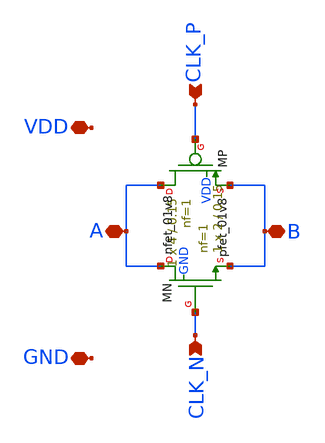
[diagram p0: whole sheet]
** sch_path: blocks/05_Switch_Network/xschem/TG_SC.sch
**.subckt TG_SC A B CLK_P CLK_N VDD GND
*.iopin A
*.iopin B
*.ipin CLK_P
*.ipin CLK_N
*.iopin VDD
*.iopin GND
XMP A CLK_P B VDD sky130_fd_pr__pfet_01v8 L=0.15 W=4 nf=1 ad='int((1 + 1)/2) * 4 / 1 * 0.29' as='int((1 + 2)/2) * 4 / 1 * 0.29'
+ pd='2*int((1 + 1)/2) * (4 / 1 + 0.29)' ps='2*int((1 + 2)/2) * (4 / 1 + 0.29)' nrd='0.29 / 4 ' nrs='0.29 / 4 '
+ sa=0 sb=0 sd=0 mult=1 m=1
XMN A CLK_N B GND sky130_fd_pr__nfet_01v8 L=0.15 W=2 nf=1 ad='int((1 + 1)/2) * 2 / 1 * 0.29' as='int((1 + 2)/2) * 2 / 1 * 0.29'
+ pd='2*int((1 + 1)/2) * (2 / 1 + 0.29)' ps='2*int((1 + 2)/2) * (2 / 1 + 0.29)' nrd='0.29 / 2 ' nrs='0.29 / 2 '
+ sa=0 sb=0 sd=0 mult=1 m=1
**.ends
.end
